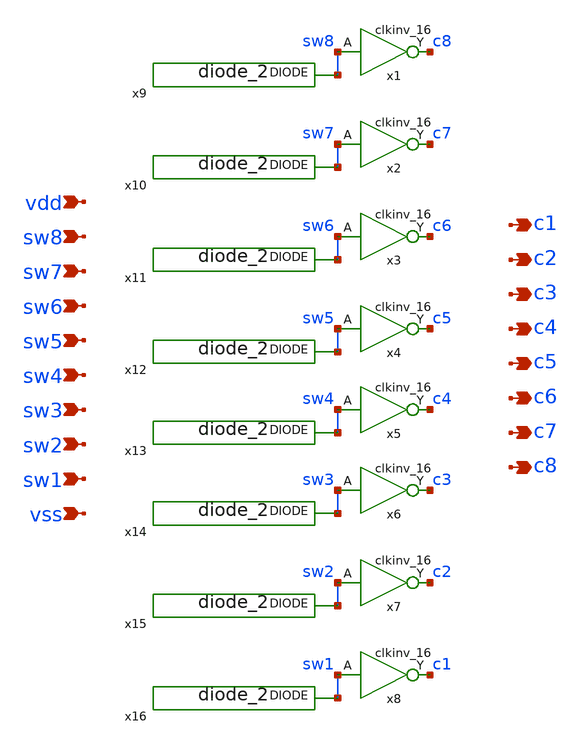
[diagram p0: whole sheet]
** sch_path: xschem/dac_sw_8b.sch
**.subckt dac_sw_8b vdd sw8 sw7 sw6 sw5 sw4 sw3 sw2 sw1 vss c8 c7 c6 c5 c4 c3 c2 c1
*.ipin vdd
*.ipin sw8
*.ipin sw7
*.ipin sw6
*.ipin sw5
*.ipin sw4
*.ipin sw3
*.ipin sw2
*.ipin sw1
*.ipin vss
*.opin c8
*.opin c7
*.opin c6
*.opin c5
*.opin c4
*.opin c3
*.opin c2
*.opin c1
x9 sw8 vss vss vdd vdd sky130_fd_sc_hd__diode_2
x10 sw7 vss vss vdd vdd sky130_fd_sc_hd__diode_2
x11 sw6 vss vss vdd vdd sky130_fd_sc_hd__diode_2
x12 sw5 vss vss vdd vdd sky130_fd_sc_hd__diode_2
x13 sw4 vss vss vdd vdd sky130_fd_sc_hd__diode_2
x14 sw3 vss vss vdd vdd sky130_fd_sc_hd__diode_2
x15 sw2 vss vss vdd vdd sky130_fd_sc_hd__diode_2
x16 sw1 vss vss vdd vdd sky130_fd_sc_hd__diode_2
x1 sw8 vss vss vdd vdd c8 sky130_fd_sc_hd__clkinv_16
x2 sw7 vss vss vdd vdd c7 sky130_fd_sc_hd__clkinv_16
x3 sw6 vss vss vdd vdd c6 sky130_fd_sc_hd__clkinv_16
x4 sw5 vss vss vdd vdd c5 sky130_fd_sc_hd__clkinv_16
x5 sw4 vss vss vdd vdd c4 sky130_fd_sc_hd__clkinv_16
x6 sw3 vss vss vdd vdd c3 sky130_fd_sc_hd__clkinv_16
x7 sw2 vss vss vdd vdd c2 sky130_fd_sc_hd__clkinv_16
x8 sw1 vss vss vdd vdd c1 sky130_fd_sc_hd__clkinv_16
**.ends
.end
